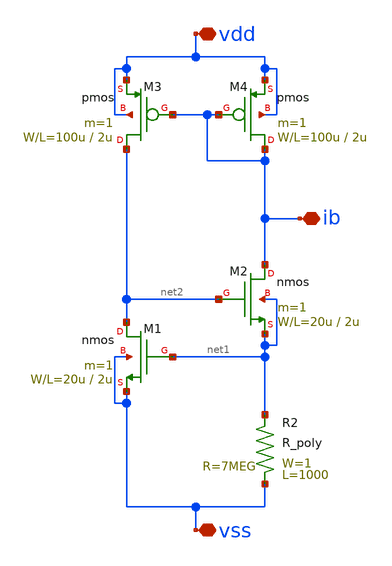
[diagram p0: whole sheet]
** sch_path: schematic/20250924_OSS_Workshop/ishikai/CS/cs-vth-ref_sym.sch
**.subckt cs-vth-ref_sym vdd vss ib
*.iopin vdd
*.iopin vss
*.iopin ib
R2 vss net1 R_poly W=1 L=1000
M4 ib ib vdd vdd pmos L=2u W=100u m=1
M3 net2 ib vdd vdd pmos L=2u W=100u m=1
M2 ib net2 net1 net1 nmos L=2u W=20u m=1
M1 net2 net1 vss vss nmos L=2u W=20u m=1
**.ends
.end
